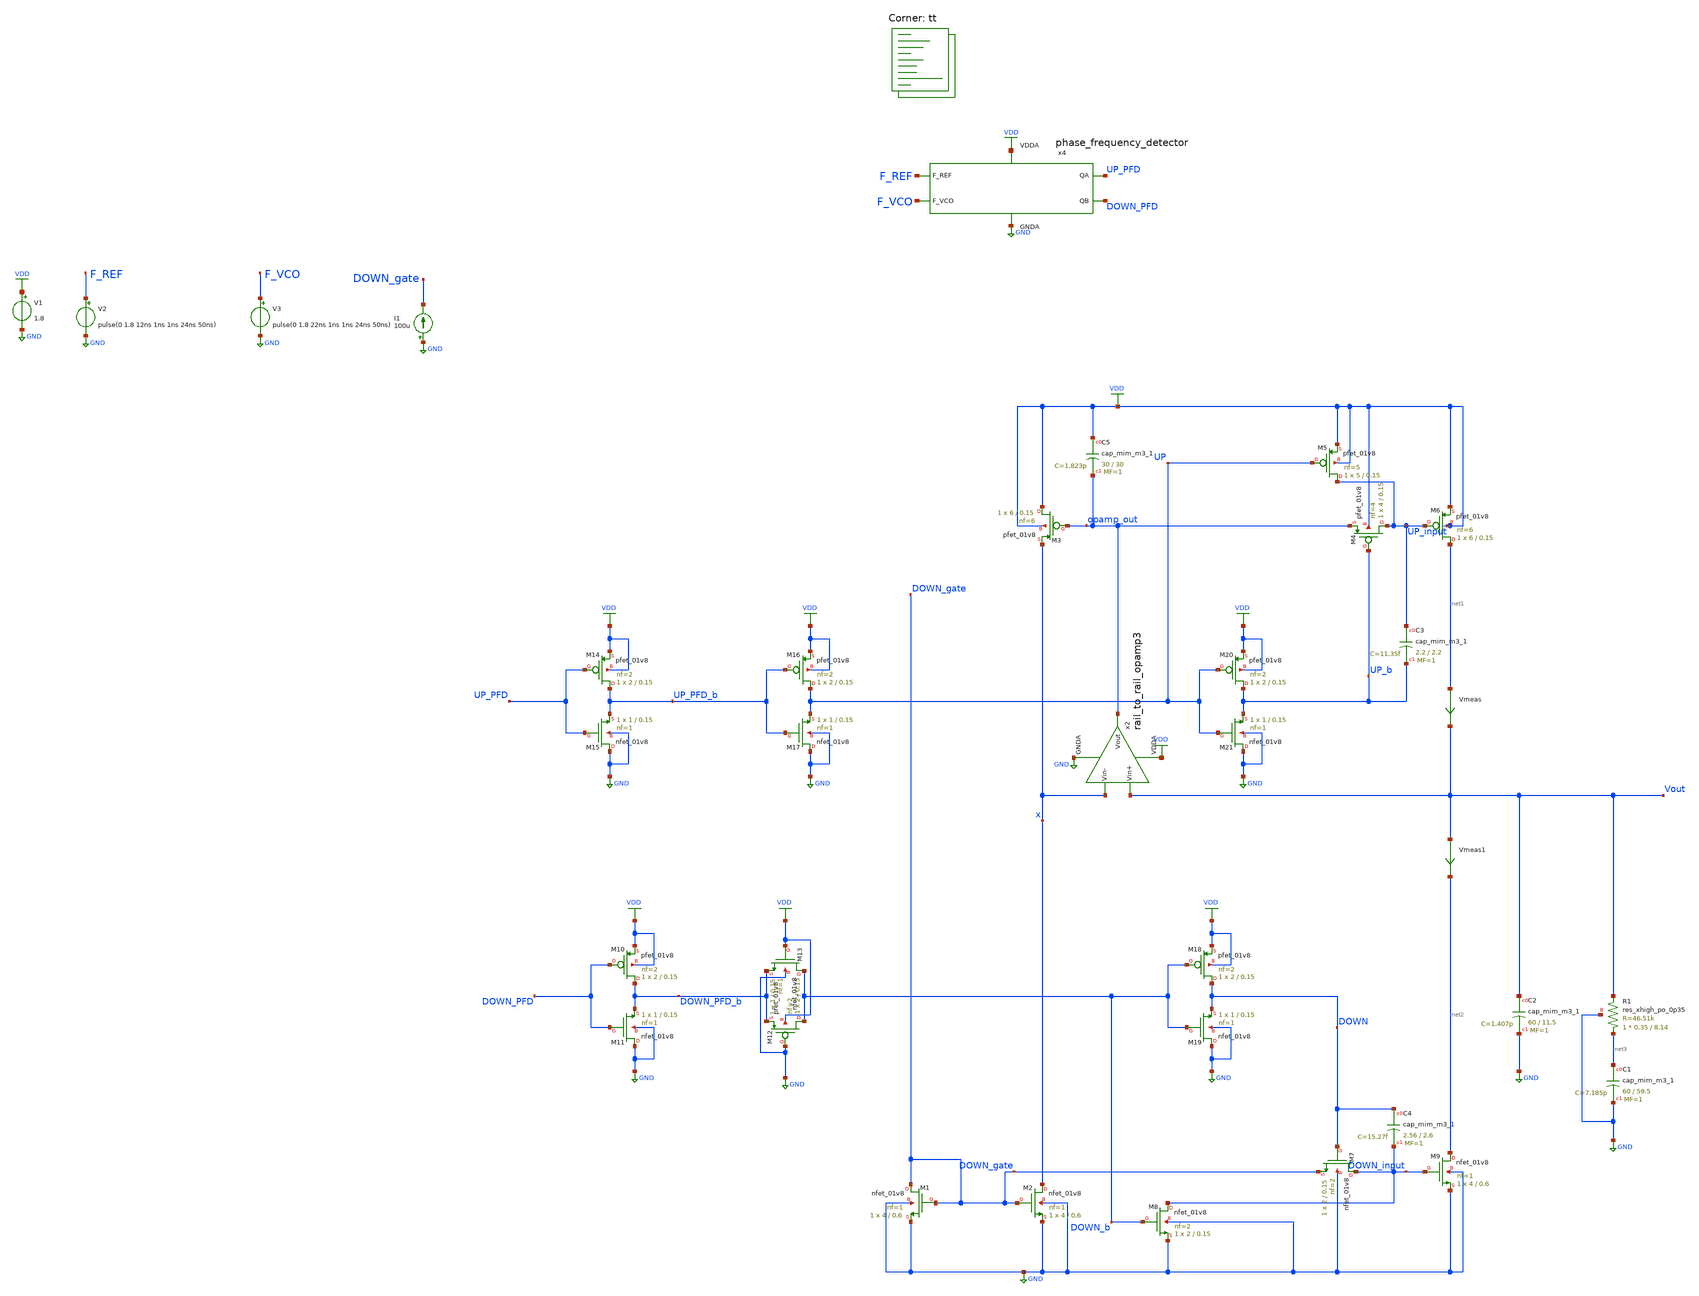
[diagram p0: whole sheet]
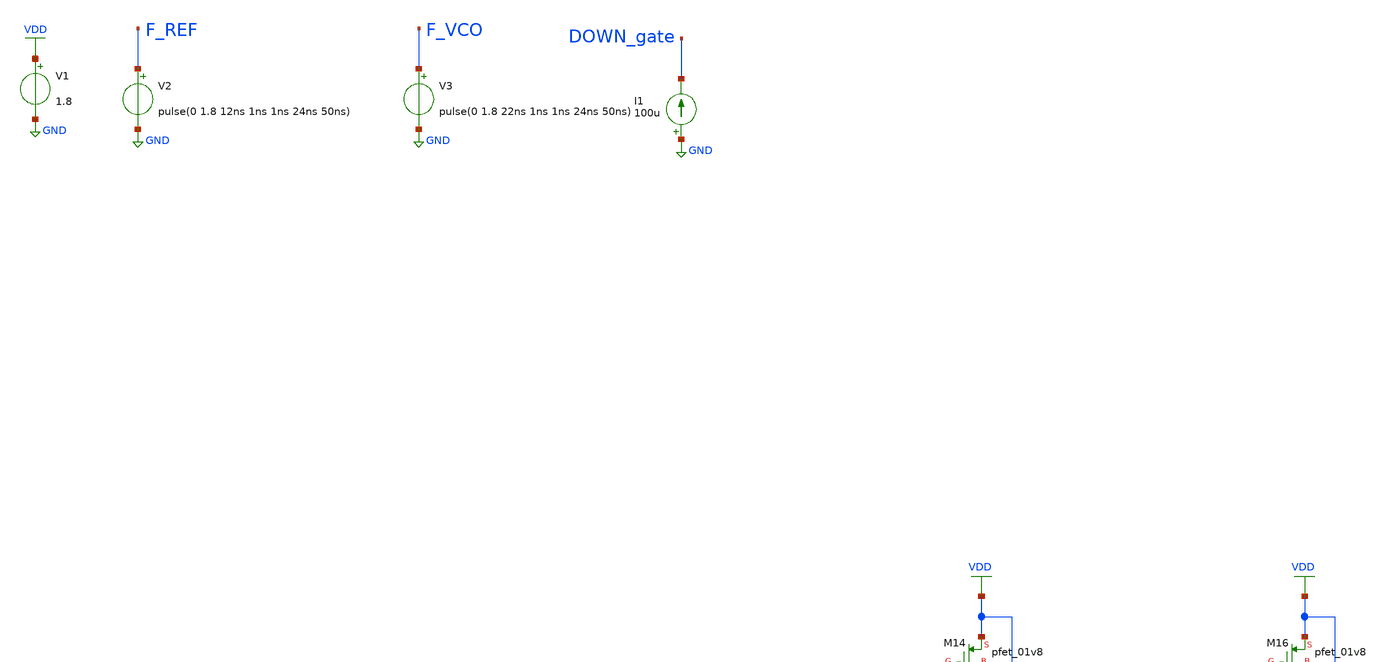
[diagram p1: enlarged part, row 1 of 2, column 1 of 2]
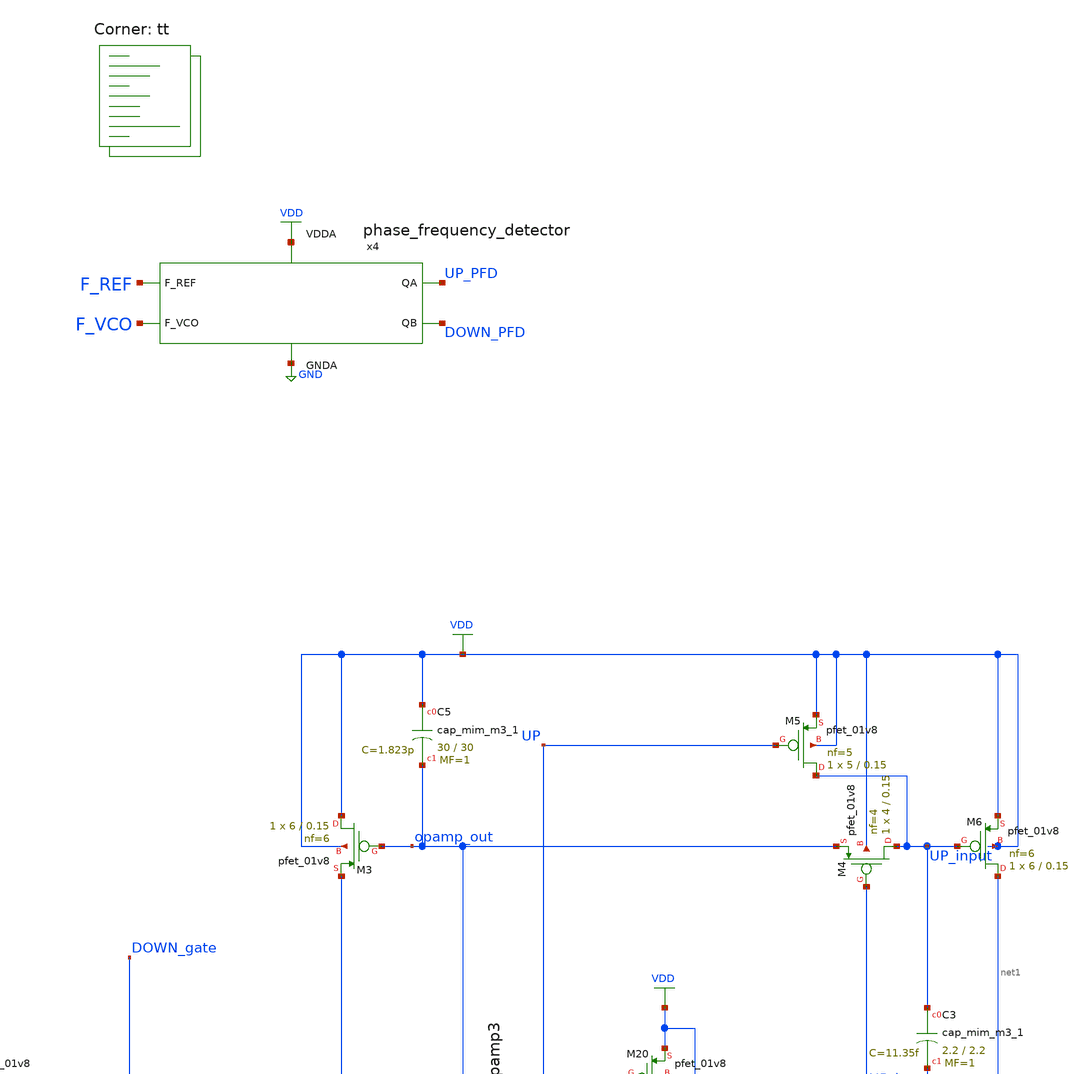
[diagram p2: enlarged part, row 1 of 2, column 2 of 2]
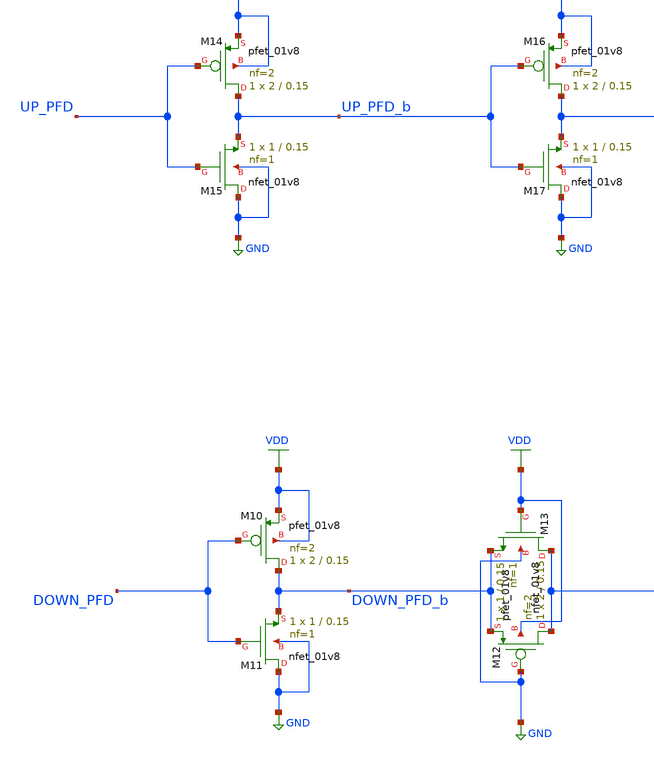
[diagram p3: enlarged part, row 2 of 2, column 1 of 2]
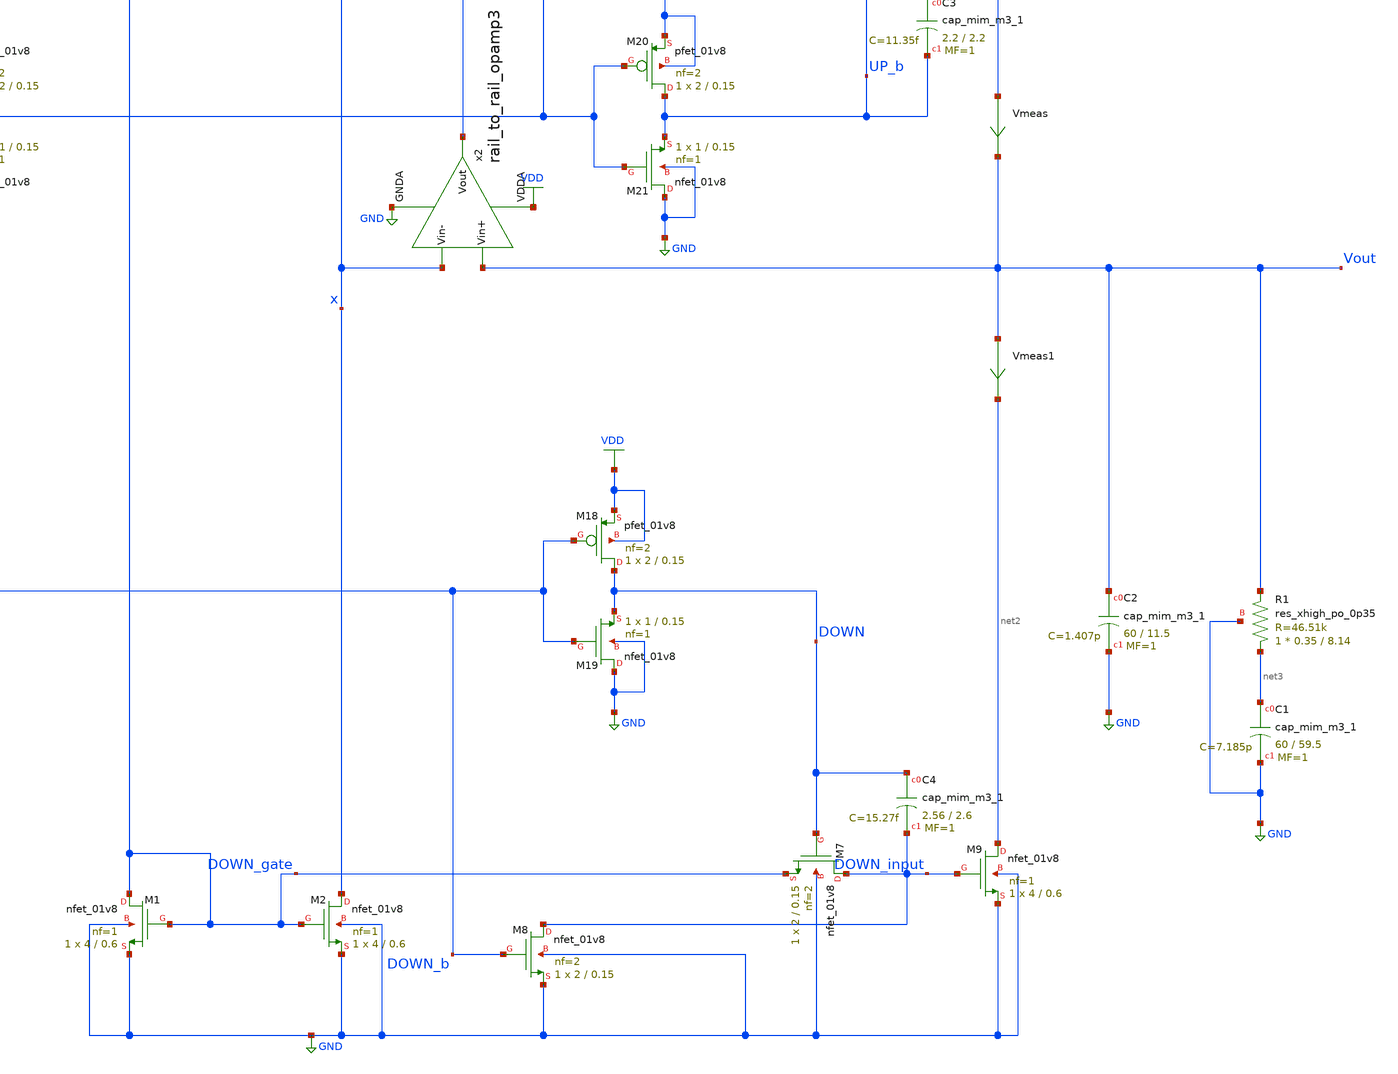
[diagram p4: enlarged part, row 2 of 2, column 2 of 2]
** sch_path: projects/pll/charge_pump/xschem_ngspice/pfd_charge_pump_8.sch
**.subckt pfd_charge_pump_8
XM1 DOWN_gate DOWN_gate GND GND sky130_fd_pr__nfet_01v8 L=0.6 W=4 nf=1 ad='int((nf+1)/2) * W/nf * 0.29'
+ as='int((nf+2)/2) * W/nf * 0.29' pd='2*int((nf+1)/2) * (W/nf + 0.29)' ps='2*int((nf+2)/2) * (W/nf + 0.29)'
+ nrd='0.29 / W' nrs='0.29 / W' sa=0 sb=0 sd=0 mult=1 m=1
XM2 x DOWN_gate GND GND sky130_fd_pr__nfet_01v8 L=0.6 W=4 nf=1 ad='int((nf+1)/2) * W/nf * 0.29' as='int((nf+2)/2) * W/nf * 0.29'
+ pd='2*int((nf+1)/2) * (W/nf + 0.29)' ps='2*int((nf+2)/2) * (W/nf + 0.29)' nrd='0.29 / W' nrs='0.29 / W'
+ sa=0 sb=0 sd=0 mult=1 m=1
XM3 VDD opamp_out x VDD sky130_fd_pr__pfet_01v8 L=0.15 W=6 nf=6 ad='int((nf+1)/2) * W/nf * 0.29' as='int((nf+2)/2) * W/nf * 0.29'
+ pd='2*int((nf+1)/2) * (W/nf + 0.29)' ps='2*int((nf+2)/2) * (W/nf + 0.29)' nrd='0.29 / W' nrs='0.29 / W'
+ sa=0 sb=0 sd=0 mult=1 m=1
V1 VDD GND 1.8
XM4 UP_input UP_b opamp_out VDD sky130_fd_pr__pfet_01v8 L=0.15 W=4 nf=4 ad='int((nf+1)/2) * W/nf * 0.29'
+ as='int((nf+2)/2) * W/nf * 0.29' pd='2*int((nf+1)/2) * (W/nf + 0.29)' ps='2*int((nf+2)/2) * (W/nf + 0.29)'
+ nrd='0.29 / W' nrs='0.29 / W' sa=0 sb=0 sd=0 mult=1 m=1
XM5 UP_input UP VDD VDD sky130_fd_pr__pfet_01v8 L=0.15 W=5 nf=5 ad='int((nf+1)/2) * W/nf * 0.29' as='int((nf+2)/2) * W/nf * 0.29'
+ pd='2*int((nf+1)/2) * (W/nf + 0.29)' ps='2*int((nf+2)/2) * (W/nf + 0.29)' nrd='0.29 / W' nrs='0.29 / W'
+ sa=0 sb=0 sd=0 mult=1 m=1
XM6 net1 UP_input VDD VDD sky130_fd_pr__pfet_01v8 L=0.15 W=6 nf=6 ad='int((nf+1)/2) * W/nf * 0.29' as='int((nf+2)/2) * W/nf * 0.29'
+ pd='2*int((nf+1)/2) * (W/nf + 0.29)' ps='2*int((nf+2)/2) * (W/nf + 0.29)' nrd='0.29 / W' nrs='0.29 / W'
+ sa=0 sb=0 sd=0 mult=1 m=1
XM7 DOWN_input DOWN DOWN_gate GND sky130_fd_pr__nfet_01v8 L=0.15 W=2 nf=2 ad='int((nf+1)/2) * W/nf * 0.29'
+ as='int((nf+2)/2) * W/nf * 0.29' pd='2*int((nf+1)/2) * (W/nf + 0.29)' ps='2*int((nf+2)/2) * (W/nf + 0.29)'
+ nrd='0.29 / W' nrs='0.29 / W' sa=0 sb=0 sd=0 mult=1 m=1
XM8 DOWN_input DOWN_b GND GND sky130_fd_pr__nfet_01v8 L=0.15 W=2 nf=2 ad='int((nf+1)/2) * W/nf * 0.29'
+ as='int((nf+2)/2) * W/nf * 0.29' pd='2*int((nf+1)/2) * (W/nf + 0.29)' ps='2*int((nf+2)/2) * (W/nf + 0.29)'
+ nrd='0.29 / W' nrs='0.29 / W' sa=0 sb=0 sd=0 mult=1 m=1
XM9 net2 DOWN_input GND GND sky130_fd_pr__nfet_01v8 L=0.6 W=4 nf=1 ad='int((nf+1)/2) * W/nf * 0.29' as='int((nf+2)/2) * W/nf * 0.29'
+ pd='2*int((nf+1)/2) * (W/nf + 0.29)' ps='2*int((nf+2)/2) * (W/nf + 0.29)' nrd='0.29 / W' nrs='0.29 / W'
+ sa=0 sb=0 sd=0 mult=1 m=1
XC2 Vout GND sky130_fd_pr__cap_mim_m3_1 W=60 L=11.5 MF=1 m=1
XC1 net3 GND sky130_fd_pr__cap_mim_m3_1 W=60 L=59.5 MF=1 m=1
V2 F_REF GND pulse(0 1.8 12ns 1ns 1ns 24ns 50ns)
V3 F_VCO GND pulse(0 1.8 22ns 1ns 1ns 24ns 50ns)
x4 F_REF F_VCO VDD UP_PFD DOWN_PFD GND phase_frequency_detector
x2 VDD Vout x opamp_out GND rail_to_rail_opamp3
XR1 net3 Vout GND sky130_fd_pr__res_xhigh_po_0p35 L=8.14 mult=1 m=1
XM12 DOWN_b GND DOWN_PFD_b VDD sky130_fd_pr__pfet_01v8 L=0.15 W=2 nf=2 ad='int((nf+1)/2) * W/nf * 0.29'
+ as='int((nf+2)/2) * W/nf * 0.29' pd='2*int((nf+1)/2) * (W/nf + 0.29)' ps='2*int((nf+2)/2) * (W/nf + 0.29)'
+ nrd='0.29 / W' nrs='0.29 / W' sa=0 sb=0 sd=0 mult=1 m=1
XM13 DOWN_b VDD DOWN_PFD_b GND sky130_fd_pr__nfet_01v8 L=0.15 W=1 nf=1 ad='int((nf+1)/2) * W/nf * 0.29'
+ as='int((nf+2)/2) * W/nf * 0.29' pd='2*int((nf+1)/2) * (W/nf + 0.29)' ps='2*int((nf+2)/2) * (W/nf + 0.29)'
+ nrd='0.29 / W' nrs='0.29 / W' sa=0 sb=0 sd=0 mult=1 m=1
XC5 VDD opamp_out sky130_fd_pr__cap_mim_m3_1 W=30 L=30 MF=1 m=1
XM10 DOWN_PFD_b DOWN_PFD VDD VDD sky130_fd_pr__pfet_01v8 L=0.15 W=2 nf=2 ad='int((nf+1)/2) * W/nf * 0.29'
+ as='int((nf+2)/2) * W/nf * 0.29' pd='2*int((nf+1)/2) * (W/nf + 0.29)' ps='2*int((nf+2)/2) * (W/nf + 0.29)'
+ nrd='0.29 / W' nrs='0.29 / W' sa=0 sb=0 sd=0 mult=1 m=1
XM11 GND DOWN_PFD DOWN_PFD_b GND sky130_fd_pr__nfet_01v8 L=0.15 W=1 nf=1 ad='int((nf+1)/2) * W/nf * 0.29'
+ as='int((nf+2)/2) * W/nf * 0.29' pd='2*int((nf+1)/2) * (W/nf + 0.29)' ps='2*int((nf+2)/2) * (W/nf + 0.29)'
+ nrd='0.29 / W' nrs='0.29 / W' sa=0 sb=0 sd=0 mult=1 m=1
XM14 UP_PFD_b UP_PFD VDD VDD sky130_fd_pr__pfet_01v8 L=0.15 W=2 nf=2 ad='int((nf+1)/2) * W/nf * 0.29'
+ as='int((nf+2)/2) * W/nf * 0.29' pd='2*int((nf+1)/2) * (W/nf + 0.29)' ps='2*int((nf+2)/2) * (W/nf + 0.29)'
+ nrd='0.29 / W' nrs='0.29 / W' sa=0 sb=0 sd=0 mult=1 m=1
XM15 GND UP_PFD UP_PFD_b GND sky130_fd_pr__nfet_01v8 L=0.15 W=1 nf=1 ad='int((nf+1)/2) * W/nf * 0.29'
+ as='int((nf+2)/2) * W/nf * 0.29' pd='2*int((nf+1)/2) * (W/nf + 0.29)' ps='2*int((nf+2)/2) * (W/nf + 0.29)'
+ nrd='0.29 / W' nrs='0.29 / W' sa=0 sb=0 sd=0 mult=1 m=1
XM16 UP UP_PFD_b VDD VDD sky130_fd_pr__pfet_01v8 L=0.15 W=2 nf=2 ad='int((nf+1)/2) * W/nf * 0.29' as='int((nf+2)/2) * W/nf * 0.29'
+ pd='2*int((nf+1)/2) * (W/nf + 0.29)' ps='2*int((nf+2)/2) * (W/nf + 0.29)' nrd='0.29 / W' nrs='0.29 / W'
+ sa=0 sb=0 sd=0 mult=1 m=1
XM17 GND UP_PFD_b UP GND sky130_fd_pr__nfet_01v8 L=0.15 W=1 nf=1 ad='int((nf+1)/2) * W/nf * 0.29' as='int((nf+2)/2) * W/nf * 0.29'
+ pd='2*int((nf+1)/2) * (W/nf + 0.29)' ps='2*int((nf+2)/2) * (W/nf + 0.29)' nrd='0.29 / W' nrs='0.29 / W'
+ sa=0 sb=0 sd=0 mult=1 m=1
XM18 DOWN DOWN_b VDD VDD sky130_fd_pr__pfet_01v8 L=0.15 W=2 nf=2 ad='int((nf+1)/2) * W/nf * 0.29' as='int((nf+2)/2) * W/nf * 0.29'
+ pd='2*int((nf+1)/2) * (W/nf + 0.29)' ps='2*int((nf+2)/2) * (W/nf + 0.29)' nrd='0.29 / W' nrs='0.29 / W'
+ sa=0 sb=0 sd=0 mult=1 m=1
XM19 GND DOWN_b DOWN GND sky130_fd_pr__nfet_01v8 L=0.15 W=1 nf=1 ad='int((nf+1)/2) * W/nf * 0.29' as='int((nf+2)/2) * W/nf * 0.29'
+ pd='2*int((nf+1)/2) * (W/nf + 0.29)' ps='2*int((nf+2)/2) * (W/nf + 0.29)' nrd='0.29 / W' nrs='0.29 / W'
+ sa=0 sb=0 sd=0 mult=1 m=1
XM20 UP_b UP VDD VDD sky130_fd_pr__pfet_01v8 L=0.15 W=2 nf=2 ad='int((nf+1)/2) * W/nf * 0.29' as='int((nf+2)/2) * W/nf * 0.29'
+ pd='2*int((nf+1)/2) * (W/nf + 0.29)' ps='2*int((nf+2)/2) * (W/nf + 0.29)' nrd='0.29 / W' nrs='0.29 / W'
+ sa=0 sb=0 sd=0 mult=1 m=1
XM21 GND UP UP_b GND sky130_fd_pr__nfet_01v8 L=0.15 W=1 nf=1 ad='int((nf+1)/2) * W/nf * 0.29' as='int((nf+2)/2) * W/nf * 0.29'
+ pd='2*int((nf+1)/2) * (W/nf + 0.29)' ps='2*int((nf+2)/2) * (W/nf + 0.29)' nrd='0.29 / W' nrs='0.29 / W'
+ sa=0 sb=0 sd=0 mult=1 m=1
I1 GND DOWN_gate 100u
Vmeas net1 Vout 0
.save i(vmeas)
Vmeas1 Vout net2 0
.save i(vmeas1)
XC3 UP_input UP_b sky130_fd_pr__cap_mim_m3_1 W=2.2 L=2.2 MF=1 m=1
XC4 DOWN DOWN_input sky130_fd_pr__cap_mim_m3_1 W=2.56 L=2.6 MF=1 m=1
**** begin user architecture code
.lib $::SKYWATER_MODELS/sky130.lib.spice tt



.include /foss/pdks/sky130A/libs.ref/sky130_fd_sc_hd/spice/sky130_fd_sc_hd.spice

.option method=gear
.option wnflag=1
* .option savecurrents

* .temp = 75

* .ic v(vout) = 1.8
* .ic v(vout) = 0.875
.ic v(vout) = 0.9

.save  v(up_pfd) v(down_pfd) v(up_pfd_b) v(down_pfd_b) v(up) v(up_b) v(down) v(down_b) v(v2) v(x) v(y) v(z) v(vout) v(up_input) v(down_input) v(down_gate) v(opamp_out) v(x2.p_bias) v(x2.n_bias) v(x2.v_common_p) v(x2.v_common_n) v(x2.p_left) v(x2.p_right) v(x2.n_left) v(x2.n_right) v(f_ref) v(f_vco) v(x4.qa) v(x4.qa_b) v(x4.qb) v(x4.qb_b) v(x4.qa) v(x4.e) v(x4.e_b) v(x4.f) v(x4.f_b) v(x4.before_reset) v(x4.reset) @m.xm6.msky130_fd_pr__pfet_01v8[id] @m.xm9.msky130_fd_pr__nfet_01v8[id]


.control
  * save v(up_pfd) v(down_pfd) v(up_pfd_b) v(down_pfd_b) v(up) v(up_b) v(down) v(down_b) v(x)
+ v(vout) v(up_input) v(down_input)
  * save all

  tran 50ps 0.5us
  * dc v2 0 1.8 0.01
  remzerovec
  write pfd_charge_pump_8_2.raw
  * wrdata /foss/designs/my_design/projects/pll/charge_pump/xschem_ngspice/pfd_charge_pump_7_QA.txt
+ v(osc)
  set appendwrite

.endc






**** end user architecture code
**.ends

* expanding   symbol:
*+  /foss/designs/my_design/projects/pll/pfd/xschem_ngspice/phase_frequency_detector.sym # of pins=6
** sym_path: projects/pll/pfd/xschem_ngspice/phase_frequency_detector.sym
** sch_path: projects/pll/pfd/xschem_ngspice/phase_frequency_detector.sch
.subckt phase_frequency_detector F_REF F_VCO VDDA QA QB GNDA
*.ipin F_REF
*.opin QA
*.ipin F_VCO
*.opin QB
*.ipin VDDA
*.ipin GNDA
x1 F_REF QA GNDA GNDA VDDA VDDA QA_b sky130_fd_sc_hd__nor2_1
x2 QA_b E GNDA GNDA VDDA VDDA QA sky130_fd_sc_hd__nor2_1
x3 QA_b E_b GNDA GNDA VDDA VDDA E sky130_fd_sc_hd__nor2_1
x4 E Reset GNDA GNDA VDDA VDDA E_b sky130_fd_sc_hd__nor2_1
x5 F_VCO QB GNDA GNDA VDDA VDDA QB_b sky130_fd_sc_hd__nor2_1
x6 QB_b F GNDA GNDA VDDA VDDA QB sky130_fd_sc_hd__nor2_1
x7 QB_b F_b GNDA GNDA VDDA VDDA F sky130_fd_sc_hd__nor2_1
x8 F Reset GNDA GNDA VDDA VDDA F_b sky130_fd_sc_hd__nor2_1
x9 QA QB GNDA GNDA VDDA VDDA before_Reset sky130_fd_sc_hd__nand2_1
x10 before_Reset GNDA GNDA VDDA VDDA net1 sky130_fd_sc_hd__inv_1
x11 net1 GNDA GNDA VDDA VDDA net2 sky130_fd_sc_hd__inv_1
x12 net2 GNDA GNDA VDDA VDDA net3 sky130_fd_sc_hd__inv_1
x13 net3 GNDA GNDA VDDA VDDA net4 sky130_fd_sc_hd__inv_1
x14 net4 GNDA GNDA VDDA VDDA Reset sky130_fd_sc_hd__inv_1
.ends


* expanding   symbol:
*+  /foss/designs/my_design/projects/pll/charge_pump/xschem_ngspice/rail_to_rail_opamp3.sym # of pins=5
** sym_path: projects/pll/charge_pump/xschem_ngspice/rail_to_rail_opamp3.sym
** sch_path: projects/pll/charge_pump/xschem_ngspice/rail_to_rail_opamp3.sch
.subckt rail_to_rail_opamp3 VDDA Vin+ Vin- Vout GNDA
*.opin Vout
*.ipin Vin+
*.ipin Vin-
*.ipin VDDA
*.ipin GNDA
XM2 n_left Vin+ v_common_n GNDA sky130_fd_pr__nfet_01v8 L=0.15 W=1 nf=1 ad='int((nf+1)/2) * W/nf * 0.29'
+ as='int((nf+2)/2) * W/nf * 0.29' pd='2*int((nf+1)/2) * (W/nf + 0.29)' ps='2*int((nf+2)/2) * (W/nf + 0.29)'
+ nrd='0.29 / W' nrs='0.29 / W' sa=0 sb=0 sd=0 mult=1 m=1
XM3 n_right Vin- v_common_n GNDA sky130_fd_pr__nfet_01v8 L=0.15 W=1 nf=1 ad='int((nf+1)/2) * W/nf * 0.29'
+ as='int((nf+2)/2) * W/nf * 0.29' pd='2*int((nf+1)/2) * (W/nf + 0.29)' ps='2*int((nf+2)/2) * (W/nf + 0.29)'
+ nrd='0.29 / W' nrs='0.29 / W' sa=0 sb=0 sd=0 mult=1 m=1
XM5 n_left n_left VDDA VDDA sky130_fd_pr__pfet_01v8 L=0.15 W=2 nf=2 ad='int((nf+1)/2) * W/nf * 0.29'
+ as='int((nf+2)/2) * W/nf * 0.29' pd='2*int((nf+1)/2) * (W/nf + 0.29)' ps='2*int((nf+2)/2) * (W/nf + 0.29)'
+ nrd='0.29 / W' nrs='0.29 / W' sa=0 sb=0 sd=0 mult=1 m=1
XM4 n_right n_left VDDA VDDA sky130_fd_pr__pfet_01v8 L=0.15 W=2 nf=2 ad='int((nf+1)/2) * W/nf * 0.29'
+ as='int((nf+2)/2) * W/nf * 0.29' pd='2*int((nf+1)/2) * (W/nf + 0.29)' ps='2*int((nf+2)/2) * (W/nf + 0.29)'
+ nrd='0.29 / W' nrs='0.29 / W' sa=0 sb=0 sd=0 mult=1 m=1
XM6 v_common_p p_bias VDDA VDDA sky130_fd_pr__pfet_01v8 L=0.15 W=3 nf=3 ad='int((nf+1)/2) * W/nf * 0.29'
+ as='int((nf+2)/2) * W/nf * 0.29' pd='2*int((nf+1)/2) * (W/nf + 0.29)' ps='2*int((nf+2)/2) * (W/nf + 0.29)'
+ nrd='0.29 / W' nrs='0.29 / W' sa=0 sb=0 sd=0 mult=1 m=1
XM7 p_left Vin+ v_common_p VDDA sky130_fd_pr__pfet_01v8 L=0.15 W=2 nf=2 ad='int((nf+1)/2) * W/nf * 0.29'
+ as='int((nf+2)/2) * W/nf * 0.29' pd='2*int((nf+1)/2) * (W/nf + 0.29)' ps='2*int((nf+2)/2) * (W/nf + 0.29)'
+ nrd='0.29 / W' nrs='0.29 / W' sa=0 sb=0 sd=0 mult=1 m=1
XM8 p_right Vin- v_common_p VDDA sky130_fd_pr__pfet_01v8 L=0.15 W=2 nf=2 ad='int((nf+1)/2) * W/nf * 0.29'
+ as='int((nf+2)/2) * W/nf * 0.29' pd='2*int((nf+1)/2) * (W/nf + 0.29)' ps='2*int((nf+2)/2) * (W/nf + 0.29)'
+ nrd='0.29 / W' nrs='0.29 / W' sa=0 sb=0 sd=0 mult=1 m=1
XM9 p_left p_left GNDA GNDA sky130_fd_pr__nfet_01v8 L=0.15 W=1 nf=1 ad='int((nf+1)/2) * W/nf * 0.29'
+ as='int((nf+2)/2) * W/nf * 0.29' pd='2*int((nf+1)/2) * (W/nf + 0.29)' ps='2*int((nf+2)/2) * (W/nf + 0.29)'
+ nrd='0.29 / W' nrs='0.29 / W' sa=0 sb=0 sd=0 mult=1 m=1
XM10 p_right p_left GNDA GNDA sky130_fd_pr__nfet_01v8 L=0.15 W=1 nf=1 ad='int((nf+1)/2) * W/nf * 0.29'
+ as='int((nf+2)/2) * W/nf * 0.29' pd='2*int((nf+1)/2) * (W/nf + 0.29)' ps='2*int((nf+2)/2) * (W/nf + 0.29)'
+ nrd='0.29 / W' nrs='0.29 / W' sa=0 sb=0 sd=0 mult=1 m=1
XM1 v_common_n n_bias GNDA GNDA sky130_fd_pr__nfet_01v8 L=0.15 W=1 nf=1 ad='int((nf+1)/2) * W/nf * 0.29'
+ as='int((nf+2)/2) * W/nf * 0.29' pd='2*int((nf+1)/2) * (W/nf + 0.29)' ps='2*int((nf+2)/2) * (W/nf + 0.29)'
+ nrd='0.29 / W' nrs='0.29 / W' sa=0 sb=0 sd=0 mult=1 m=1
XM11 Vout n_right VDDA VDDA sky130_fd_pr__pfet_01v8 L=0.15 W=16 nf=2 ad='int((nf+1)/2) * W/nf * 0.29'
+ as='int((nf+2)/2) * W/nf * 0.29' pd='2*int((nf+1)/2) * (W/nf + 0.29)' ps='2*int((nf+2)/2) * (W/nf + 0.29)'
+ nrd='0.29 / W' nrs='0.29 / W' sa=0 sb=0 sd=0 mult=1 m=1
XM12 Vout p_right GNDA GNDA sky130_fd_pr__nfet_01v8 L=0.15 W=8 nf=1 ad='int((nf+1)/2) * W/nf * 0.29'
+ as='int((nf+2)/2) * W/nf * 0.29' pd='2*int((nf+1)/2) * (W/nf + 0.29)' ps='2*int((nf+2)/2) * (W/nf + 0.29)'
+ nrd='0.29 / W' nrs='0.29 / W' sa=0 sb=0 sd=0 mult=1 m=1
XM13 n_bias n_bias GNDA GNDA sky130_fd_pr__nfet_01v8 L=0.15 W=1 nf=1 ad='int((nf+1)/2) * W/nf * 0.29'
+ as='int((nf+2)/2) * W/nf * 0.29' pd='2*int((nf+1)/2) * (W/nf + 0.29)' ps='2*int((nf+2)/2) * (W/nf + 0.29)'
+ nrd='0.29 / W' nrs='0.29 / W' sa=0 sb=0 sd=0 mult=1 m=1
XM15 p_bias p_bias VDDA VDDA sky130_fd_pr__pfet_01v8 L=0.15 W=2 nf=2 ad='int((nf+1)/2) * W/nf * 0.29'
+ as='int((nf+2)/2) * W/nf * 0.29' pd='2*int((nf+1)/2) * (W/nf + 0.29)' ps='2*int((nf+2)/2) * (W/nf + 0.29)'
+ nrd='0.29 / W' nrs='0.29 / W' sa=0 sb=0 sd=0 mult=1 m=1
Vmeas net1 n_bias 0
.save i(vmeas)
XM14 net1 net1 p_bias p_bias sky130_fd_pr__pfet_01v8 L=0.15 W=2 nf=2 ad='int((nf+1)/2) * W/nf * 0.29'
+ as='int((nf+2)/2) * W/nf * 0.29' pd='2*int((nf+1)/2) * (W/nf + 0.29)' ps='2*int((nf+2)/2) * (W/nf + 0.29)'
+ nrd='0.29 / W' nrs='0.29 / W' sa=0 sb=0 sd=0 mult=1 m=1
.ends

.GLOBAL VDD
.GLOBAL GND
.end
